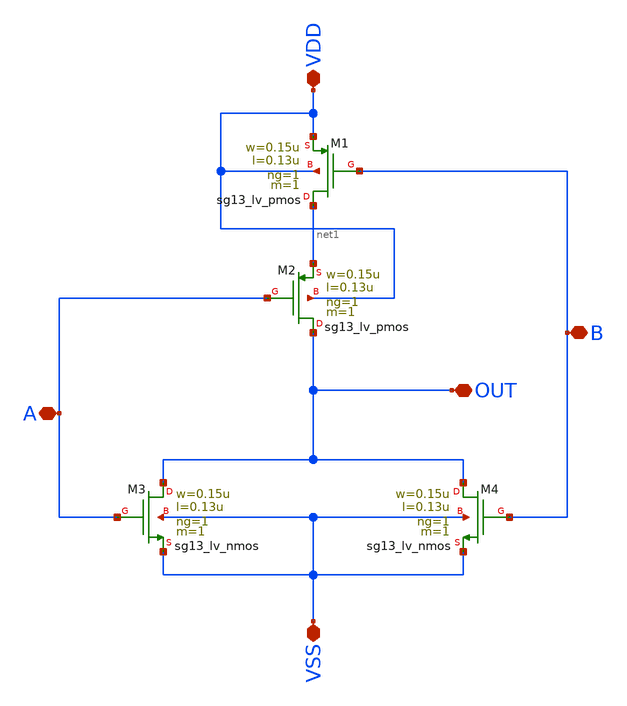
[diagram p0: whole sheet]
** sch_path: blocks/norgate/nor.sch
**.subckt nor VDD A VSS B OUT
*.iopin VDD
*.iopin A
*.iopin VSS
*.iopin B
*.iopin OUT
XM1 net1 B VDD VDD sg13_lv_pmos w=0.15u l=0.13u ng=1 m=1 mm_ok=1
XM2 OUT A net1 VDD sg13_lv_pmos w=0.15u l=0.13u ng=1 m=1 mm_ok=1
XM3 OUT A VSS VSS sg13_lv_nmos w=0.15u l=0.13u ng=1 m=1 mm_ok=1
XM4 OUT B VSS VSS sg13_lv_nmos w=0.15u l=0.13u ng=1 m=1 mm_ok=1
**.ends
.end
